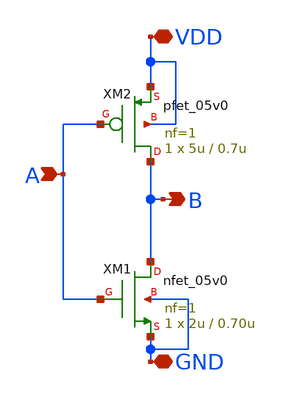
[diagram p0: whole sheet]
** sch_path: designs/libs/tb_analog/tb_inv/inv.sch
**.subckt inv A B VDD GND
*.ipin A
*.opin B
*.iopin VDD
*.iopin GND
XM1 B A GND GND nfet_05v0 L=0.70u W=2u nf=1 ad='int((nf+1)/2) * W/nf * 0.18u' as='int((nf+2)/2) * W/nf * 0.18u'
+ pd='2*int((nf+1)/2) * (W/nf + 0.18u)' ps='2*int((nf+2)/2) * (W/nf + 0.18u)' nrd='0.18u / W' nrs='0.18u / W'
+ sa=0 sb=0 sd=0 m=1
XM2 B A VDD VDD pfet_05v0 L=0.7u W=5u nf=1 ad='int((nf+1)/2) * W/nf * 0.18u' as='int((nf+2)/2) * W/nf * 0.18u'
+ pd='2*int((nf+1)/2) * (W/nf + 0.18u)' ps='2*int((nf+2)/2) * (W/nf + 0.18u)' nrd='0.18u / W' nrs='0.18u / W'
+ sa=0 sb=0 sd=0 m=1
**.ends
.end
